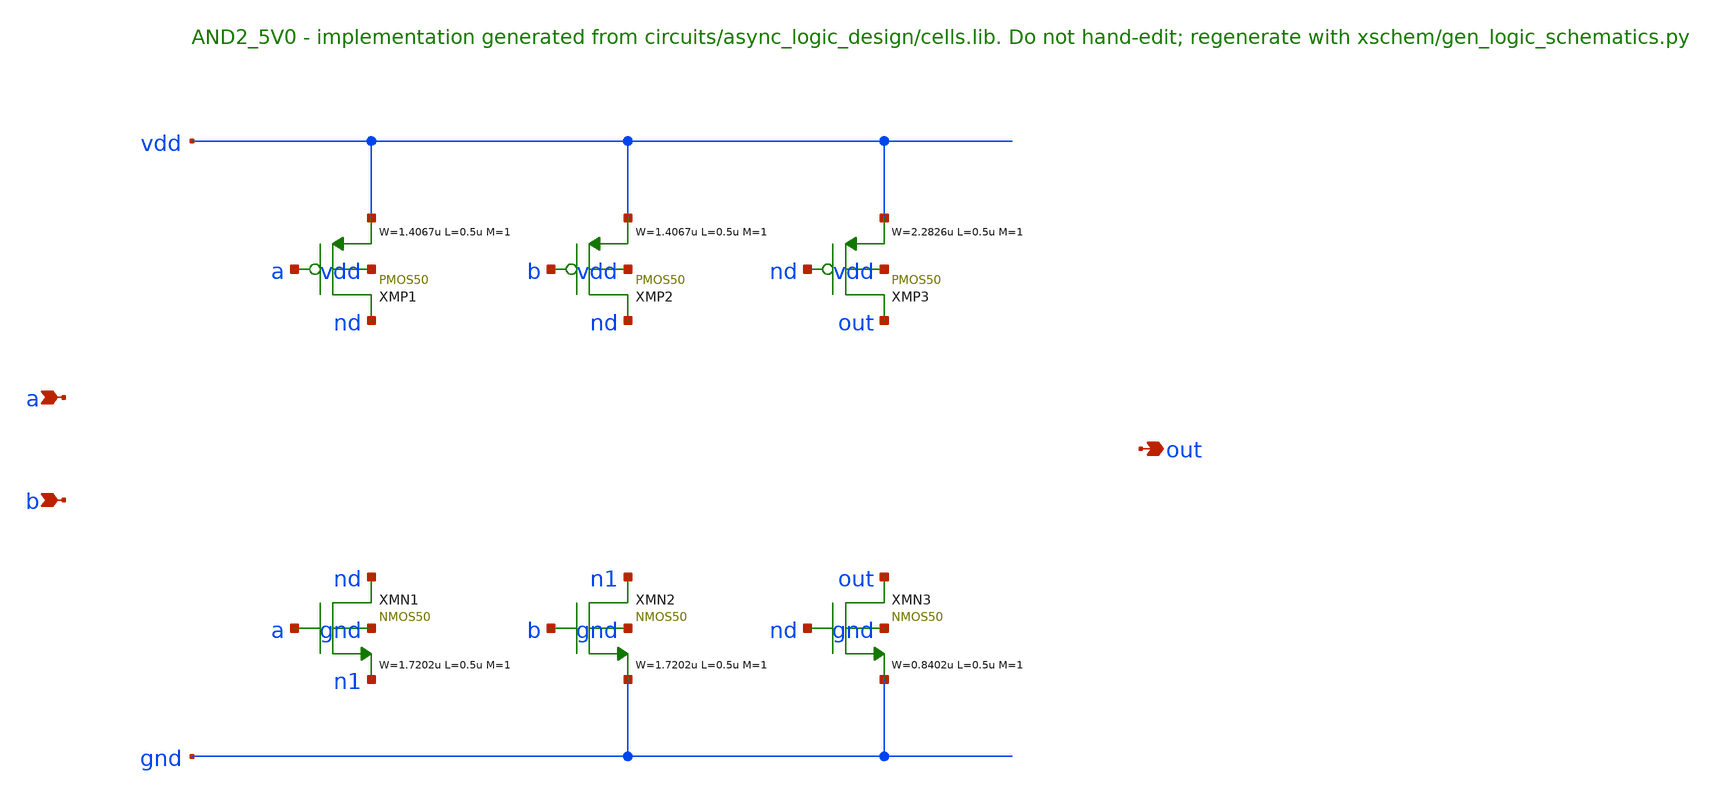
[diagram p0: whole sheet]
** sch_path: xschem/logic/AND2_5V0.sch
**.subckt AND2_5V0 a b out
*.ipin a
*.ipin b
*.opin out
XMP1 nd a vdd vdd PMOS50 W=1.4067u L=0.5u M=1 MM_SIGMA=0
XMP2 nd b vdd vdd PMOS50 W=1.4067u L=0.5u M=1 MM_SIGMA=0
XMP3 out nd vdd vdd PMOS50 W=2.2826u L=0.5u M=1 MM_SIGMA=0
XMN1 nd a n1 gnd NMOS50 W=1.7202u L=0.5u M=1 MM_SIGMA=0
XMN2 n1 b gnd gnd NMOS50 W=1.7202u L=0.5u M=1 MM_SIGMA=0
XMN3 out nd gnd gnd NMOS50 W=0.8402u L=0.5u M=1 MM_SIGMA=0
**.ends
.end
